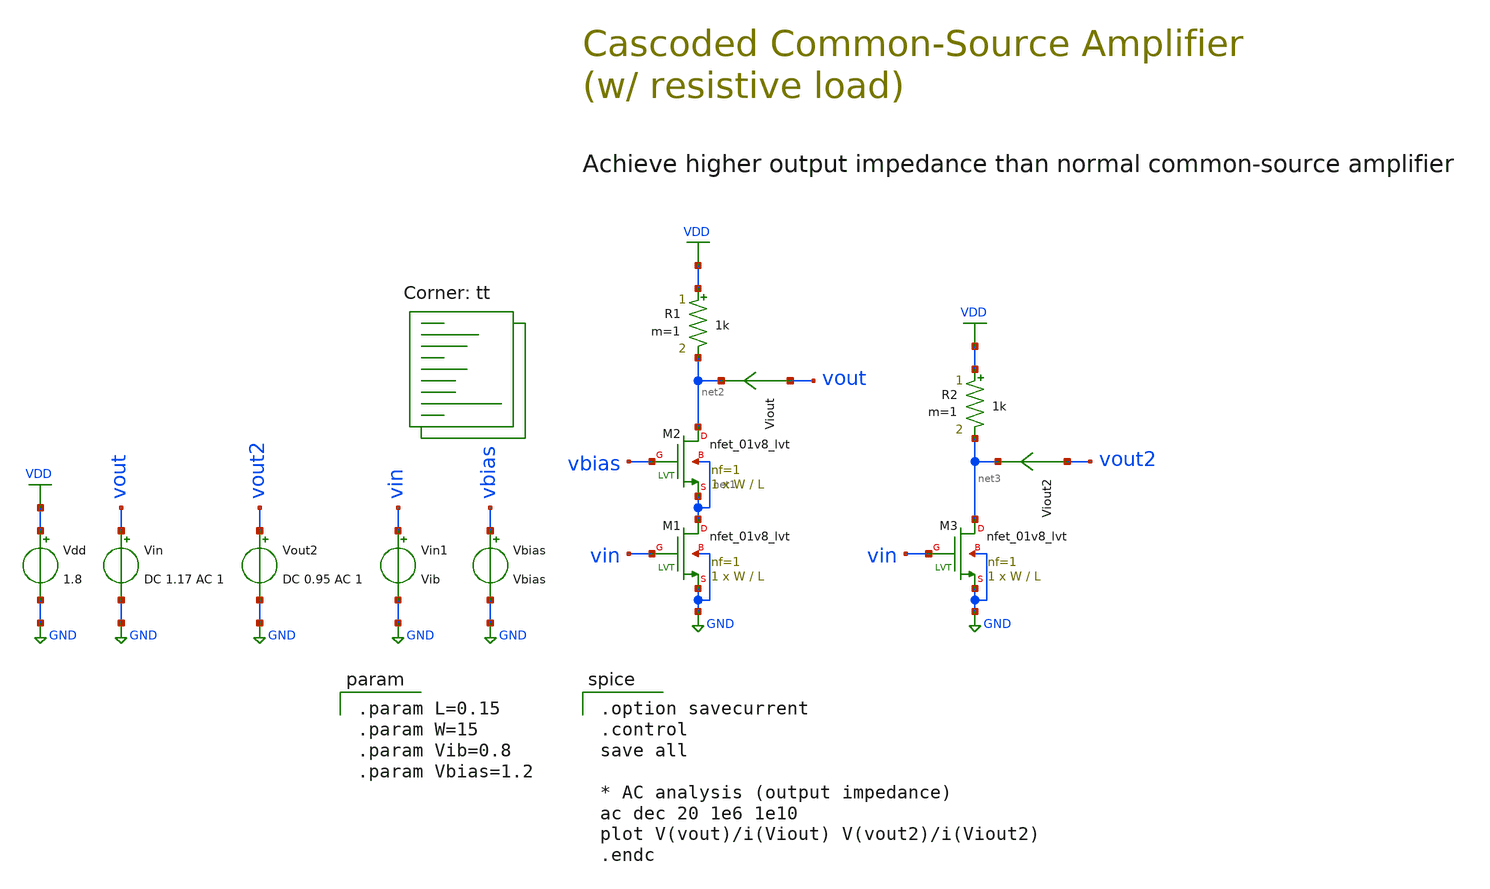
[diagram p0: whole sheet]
** sch_path: 11-b_cascoded-cs.sch
**.subckt 11-b_cascoded-cs
XM1 net1 vin GND GND sky130_fd_pr__nfet_01v8_lvt L=L W=W nf=1 ad='int((1 + 1)/2) * W / 1 * 0.29' as='int((1 + 2)/2) * W / 1 * 0.29'
+ pd='2*int((1 + 1)/2) * (W / 1 + 0.29)' ps='2*int((1 + 2)/2) * (W / 1 + 0.29)' nrd='0.29 / W ' nrs='0.29 / W '
+ sa=0 sb=0 sd=0 mult=1 m=1
Vdd VDD GND 1.8
Vin vout GND DC 1.17 AC 1
R1 VDD net2 1k m=1
XM2 net2 vbias net1 net1 sky130_fd_pr__nfet_01v8_lvt L=L W=W nf=1 ad='int((1 + 1)/2) * W / 1 * 0.29'
+ as='int((1 + 2)/2) * W / 1 * 0.29' pd='2*int((1 + 1)/2) * (W / 1 + 0.29)' ps='2*int((1 + 2)/2) * (W / 1 + 0.29)'
+ nrd='0.29 / W ' nrs='0.29 / W ' sa=0 sb=0 sd=0 mult=1 m=1
Vbias vbias GND Vbias
XM3 net3 vin GND GND sky130_fd_pr__nfet_01v8_lvt L=L W=W nf=1 ad='int((1 + 1)/2) * W / 1 * 0.29' as='int((1 + 2)/2) * W / 1 * 0.29'
+ pd='2*int((1 + 1)/2) * (W / 1 + 0.29)' ps='2*int((1 + 2)/2) * (W / 1 + 0.29)' nrd='0.29 / W ' nrs='0.29 / W '
+ sa=0 sb=0 sd=0 mult=1 m=1
R2 VDD net3 1k m=1
Viout vout net2 0
.save i(viout)
Viout2 vout2 net3 0
.save i(viout2)
Vout2 vout2 GND DC 0.95 AC 1
Vin1 vin GND Vib
**** begin user architecture code
.lib $::SKYWATER_MODELS/sky130.lib.spice tt

.param L=0.15
.param W=15
.param Vib=0.8
.param Vbias=1.2


.option savecurrent
.control
save all

* AC analysis (output impedance)
ac dec 20 1e6 1e10
plot V(vout)/i(Viout) V(vout2)/i(Viout2)
.endc

**** end user architecture code
**.ends
.GLOBAL GND
.GLOBAL VDD
.end
